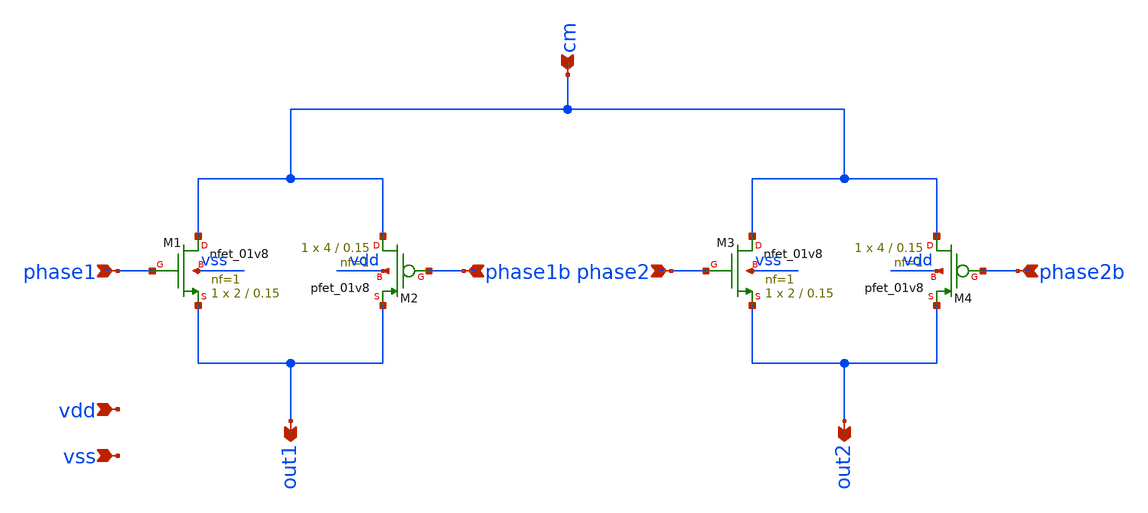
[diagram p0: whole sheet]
** sch_path: pll/pll_cp_sw_spdt/xschem/pll_cp_sw_spdt.sch
**.subckt pll_cp_sw_spdt vdd vss phase1 phase1b phase2 phase2b cm out2 out1
*.ipin vdd
*.ipin vss
*.ipin phase1
*.ipin phase1b
*.ipin phase2
*.ipin phase2b
*.ipin cm
*.opin out2
*.opin out1
XM1 cm phase1 out1 vss sky130_fd_pr__nfet_01v8 L=0.15 W=2 nf=1 ad='int((nf+1)/2) * W/nf * 0.29' as='int((nf+2)/2) * W/nf * 0.29'
+ pd='2*int((nf+1)/2) * (W/nf + 0.29)' ps='2*int((nf+2)/2) * (W/nf + 0.29)' nrd='0.29 / W' nrs='0.29 / W'
+ sa=0 sb=0 sd=0 mult=1 m=1
XM2 cm phase1b out1 vdd sky130_fd_pr__pfet_01v8 L=0.15 W=4 nf=1 ad='int((nf+1)/2) * W/nf * 0.29' as='int((nf+2)/2) * W/nf * 0.29'
+ pd='2*int((nf+1)/2) * (W/nf + 0.29)' ps='2*int((nf+2)/2) * (W/nf + 0.29)' nrd='0.29 / W' nrs='0.29 / W'
+ sa=0 sb=0 sd=0 mult=1 m=1
XM3 cm phase2 out2 vss sky130_fd_pr__nfet_01v8 L=0.15 W=2 nf=1 ad='int((nf+1)/2) * W/nf * 0.29' as='int((nf+2)/2) * W/nf * 0.29'
+ pd='2*int((nf+1)/2) * (W/nf + 0.29)' ps='2*int((nf+2)/2) * (W/nf + 0.29)' nrd='0.29 / W' nrs='0.29 / W'
+ sa=0 sb=0 sd=0 mult=1 m=1
XM4 cm phase2b out2 vdd sky130_fd_pr__pfet_01v8 L=0.15 W=4 nf=1 ad='int((nf+1)/2) * W/nf * 0.29' as='int((nf+2)/2) * W/nf * 0.29'
+ pd='2*int((nf+1)/2) * (W/nf + 0.29)' ps='2*int((nf+2)/2) * (W/nf + 0.29)' nrd='0.29 / W' nrs='0.29 / W'
+ sa=0 sb=0 sd=0 mult=1 m=1
**** begin user architecture code

.options wnflag=1
.include $::SKYWATER_MODELS/cells/nfet_01v8/sky130_fd_pr__nfet_01v8__tt.corner.spice
.include $::SKYWATER_MODELS/cells/nfet_01v8_lvt/sky130_fd_pr__nfet_01v8_lvt__tt.corner.spice
.include $::SKYWATER_MODELS/cells/pfet_01v8/sky130_fd_pr__pfet_01v8__tt.corner.spice
.include $::SKYWATER_MODELS/cells/nfet_03v3_nvt/sky130_fd_pr__nfet_03v3_nvt__tt.corner.spice
.include $::SKYWATER_MODELS/cells/nfet_05v0_nvt/sky130_fd_pr__nfet_05v0_nvt__tt.corner.spice
.include $::SKYWATER_MODELS/cells/esd_nfet_01v8/sky130_fd_pr__esd_nfet_01v8__tt.corner.spice
.include $::SKYWATER_MODELS/cells/pfet_01v8_lvt/sky130_fd_pr__pfet_01v8_lvt__tt.corner.spice
.include $::SKYWATER_MODELS/cells/pfet_01v8_hvt/sky130_fd_pr__pfet_01v8_hvt__tt.corner.spice
.include $::SKYWATER_MODELS/cells/esd_pfet_g5v0d10v5/sky130_fd_pr__esd_pfet_g5v0d10v5__tt.corner.spice
.include $::SKYWATER_MODELS/cells/pfet_g5v0d10v5/sky130_fd_pr__pfet_g5v0d10v5__tt.corner.spice
.include $::SKYWATER_MODELS/cells/pfet_g5v0d16v0/sky130_fd_pr__pfet_g5v0d16v0__tt.corner.spice
.include $::SKYWATER_MODELS/cells/nfet_g5v0d10v5/sky130_fd_pr__nfet_g5v0d10v5__tt.corner.spice
.include $::SKYWATER_MODELS/cells/nfet_g5v0d16v0/sky130_fd_pr__nfet_g5v0d16v0__tt_discrete.corner.spice
.include $::SKYWATER_MODELS/cells/esd_nfet_g5v0d10v5/sky130_fd_pr__esd_nfet_g5v0d10v5__tt.corner.spice
.include $::SKYWATER_MODELS/models/corners/tt/nonfet.spice

.include $::SKYWATER_MODELS/cells/cap_var_hvt/sky130_fd_pr__cap_var_hvt.model.spice

* Mismatch parameters
.include $::SKYWATER_MODELS/cells/nfet_01v8/sky130_fd_pr__nfet_01v8__mismatch.corner.spice
.include $::SKYWATER_MODELS/cells/pfet_01v8/sky130_fd_pr__pfet_01v8__mismatch.corner.spice
.include $::SKYWATER_MODELS/cells/nfet_01v8_lvt/sky130_fd_pr__nfet_01v8_lvt__mismatch.corner.spice
.include $::SKYWATER_MODELS/cells/pfet_01v8_lvt/sky130_fd_pr__pfet_01v8_lvt__mismatch.corner.spice
.include $::SKYWATER_MODELS/cells/pfet_01v8_hvt/sky130_fd_pr__pfet_01v8_hvt__mismatch.corner.spice
.include $::SKYWATER_MODELS/cells/nfet_g5v0d10v5/sky130_fd_pr__nfet_g5v0d10v5__mismatch.corner.spice
.include $::SKYWATER_MODELS/cells/pfet_g5v0d10v5/sky130_fd_pr__pfet_g5v0d10v5__mismatch.corner.spice
.include $::SKYWATER_MODELS/cells/nfet_05v0_nvt/sky130_fd_pr__nfet_05v0_nvt__mismatch.corner.spice
.include $::SKYWATER_MODELS/cells/nfet_03v3_nvt/sky130_fd_pr__nfet_03v3_nvt__mismatch.corner.spice

* Resistor$::SKYWATER_MODELS/Capacitor
.include $::SKYWATER_MODELS/models/r+c/res_typical__cap_typical.spice
.include $::SKYWATER_MODELS/models/r+c/res_typical__cap_typical__lin.spice

* Special cells
.include $::SKYWATER_MODELS/models/corners/tt/specialized_cells.spice

* All models
.include $::SKYWATER_MODELS/models/all.spice

* Corner
.include $::SKYWATER_MODELS/models/corners/tt/rf.spice

**** end user architecture code
**.ends
.end
